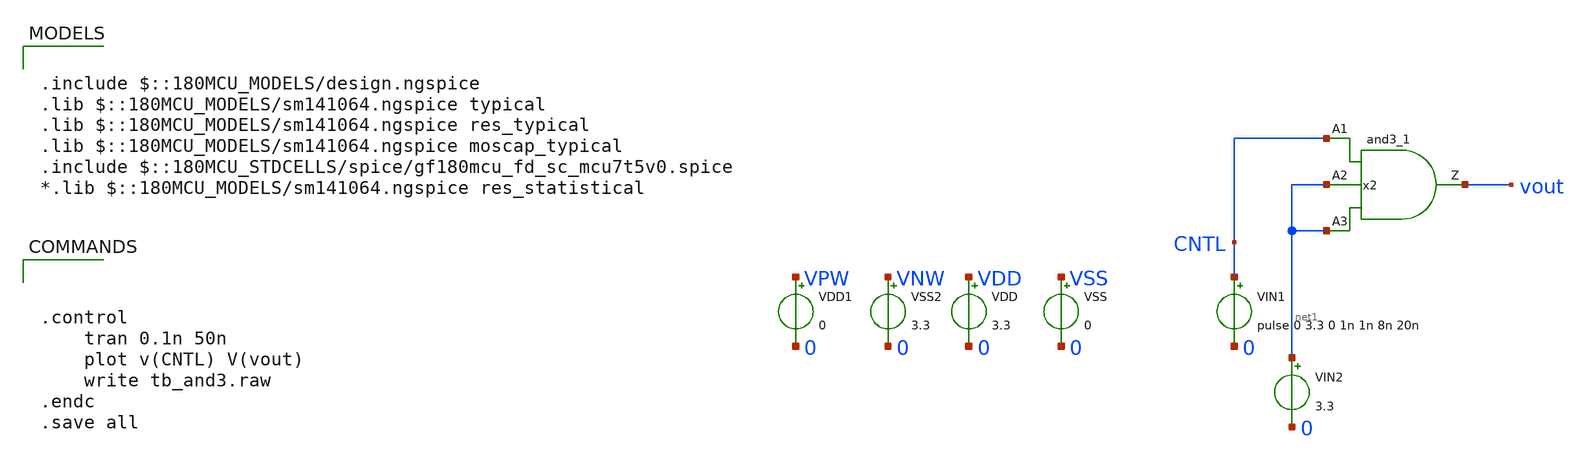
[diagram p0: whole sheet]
** sch_path: DAC/xschem/std_cell/tb/tb_and3.sch
**.subckt tb_and3
VIN1 CNTL 0 pulse 0 3.3 0 1n 1n 8n 20n
VIN2 net1 0 3.3
VDD VDD 0 3.3
VSS VSS 0 0
VDD1 VPW 0 0
VSS2 VNW 0 3.3
x2 CNTL net1 net1 vout VDD VNW VPW VSS gf180mcu_fd_sc_mcu7t5v0__and3_1
**** begin user architecture code



.control
    tran 0.1n 50n
    plot v(CNTL) V(vout)
    write tb_and3.raw
.endc
.save all




.include $::180MCU_MODELS/design.ngspice
.lib $::180MCU_MODELS/sm141064.ngspice typical
.lib $::180MCU_MODELS/sm141064.ngspice res_typical
.lib $::180MCU_MODELS/sm141064.ngspice moscap_typical
.include $::180MCU_STDCELLS/spice/gf180mcu_fd_sc_mcu7t5v0.spice
*.lib $::180MCU_MODELS/sm141064.ngspice res_statistical

**** end user architecture code
**.ends
.end
